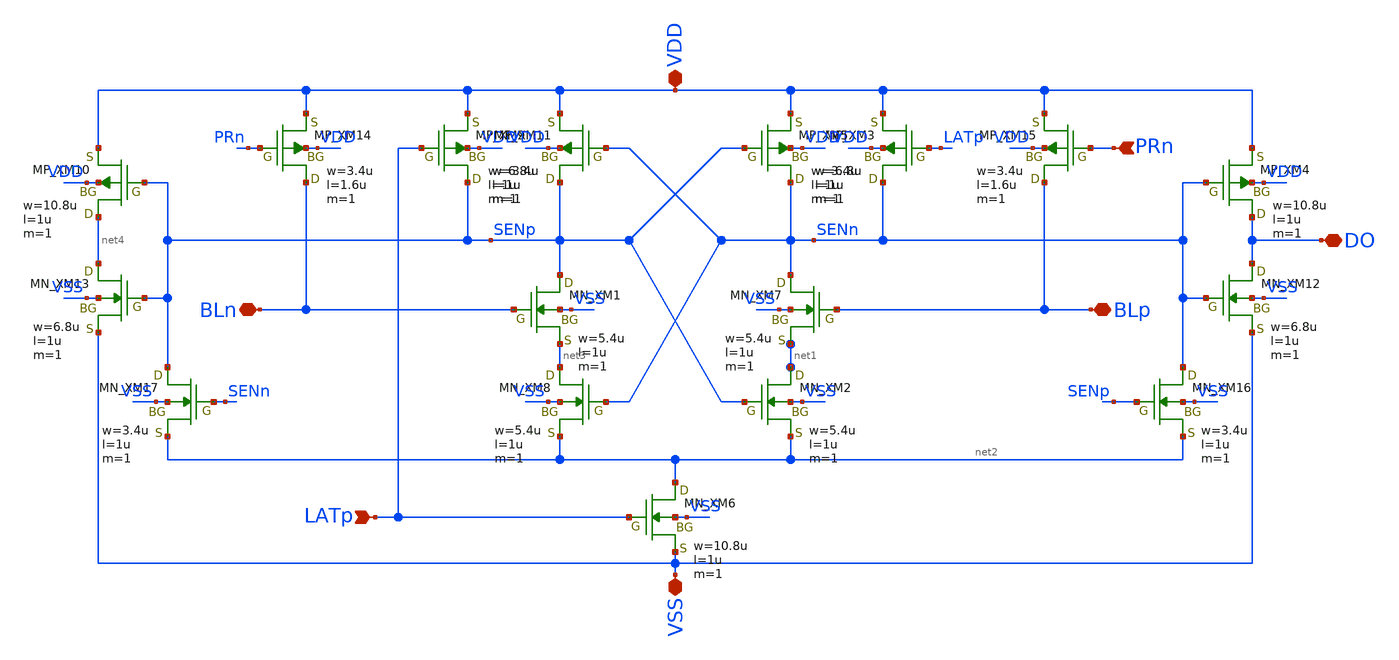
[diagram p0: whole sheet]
** sch_path: module/SRAM128/schematic/SA.sch
**.subckt SA BLp BLn LATp VDD VSS DO PRn
*.iopin BLp
*.iopin BLn
*.ipin LATp
*.iopin VDD
*.iopin VSS
*.iopin DO
*.ipin PRn
XXM1 SENp BLn net3 VSS NMOS w=5.4u l=1u as=0 ad=0 ps=0 pd=0 nrd=0 nrs=0 m=1
XXM2 net1 SENp net2 VSS NMOS w=5.4u l=1u as=0 ad=0 ps=0 pd=0 nrd=0 nrs=0 m=1
XXM3 SENn LATp VDD VDD PMOS w=6.8u l=1u as=0 ad=0 ps=0 pd=0 nrd=0 nrs=0 m=1
XXM4 DO SENn VDD VDD PMOS w=10.8u l=1u as=0 ad=0 ps=0 pd=0 nrd=0 nrs=0 m=1
XXM5 SENn SENp VDD VDD PMOS w=3.4u l=1u as=0 ad=0 ps=0 pd=0 nrd=0 nrs=0 m=1
XXM6 net2 LATp VSS VSS NMOS w=10.8u l=1u as=0 ad=0 ps=0 pd=0 nrd=0 nrs=0 m=1
XXM7 SENn BLp net1 VSS NMOS w=5.4u l=1u as=0 ad=0 ps=0 pd=0 nrd=0 nrs=0 m=1
XXM8 net3 SENn net2 VSS NMOS w=5.4u l=1u as=0 ad=0 ps=0 pd=0 nrd=0 nrs=0 m=1
XXM9 SENp LATp VDD VDD PMOS w=6.8u l=1u as=0 ad=0 ps=0 pd=0 nrd=0 nrs=0 m=1
XXM11 SENp SENn VDD VDD PMOS w=3.4u l=1u as=0 ad=0 ps=0 pd=0 nrd=0 nrs=0 m=1
XXM12 DO SENn VSS VSS NMOS w=6.8u l=1u as=0 ad=0 ps=0 pd=0 nrd=0 nrs=0 m=1
XXM10 net4 SENp VDD VDD PMOS w=10.8u l=1u as=0 ad=0 ps=0 pd=0 nrd=0 nrs=0 m=1
XXM13 net4 SENp VSS VSS NMOS w=6.8u l=1u as=0 ad=0 ps=0 pd=0 nrd=0 nrs=0 m=1
XXM14 BLn PRn VDD VDD PMOS w=3.4u l=1.6u as=0 ad=0 ps=0 pd=0 nrd=0 nrs=0 m=1
XXM15 BLp PRn VDD VDD PMOS w=3.4u l=1.6u as=0 ad=0 ps=0 pd=0 nrd=0 nrs=0 m=1
XXM16 SENn SENp net2 VSS NMOS w=3.4u l=1u as=0 ad=0 ps=0 pd=0 nrd=0 nrs=0 m=1
XXM17 SENp SENn net2 VSS NMOS w=3.4u l=1u as=0 ad=0 ps=0 pd=0 nrd=0 nrs=0 m=1
**.ends
.end
